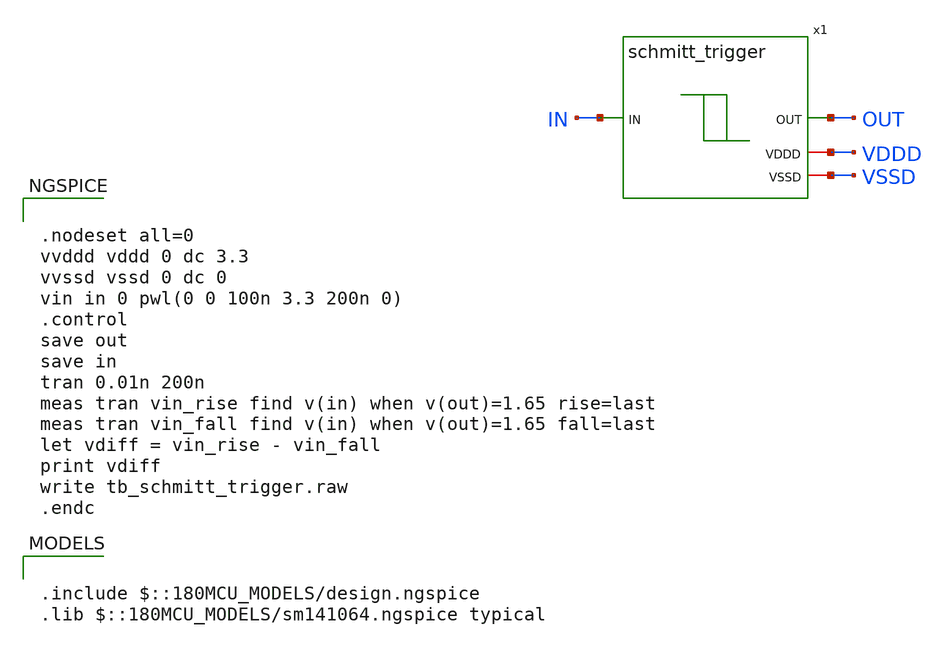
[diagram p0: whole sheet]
** sch_path: designs/libs/tb_switch_matrix/tb_schmitt_trigger.sch
**.subckt tb_schmitt_trigger
x1 IN OUT VDDD VSSD schmitt_trigger
**** begin user architecture code

.include $::180MCU_MODELS/design.ngspice
.lib $::180MCU_MODELS/sm141064.ngspice typical



.nodeset all=0
vvddd vddd 0 dc 3.3
vvssd vssd 0 dc 0
vin in 0 pwl(0 0 100n 3.3 200n 0)
.control
save out
save in
tran 0.01n 200n
meas tran vin_rise find v(in) when v(out)=1.65 rise=last
meas tran vin_fall find v(in) when v(out)=1.65 fall=last
let vdiff = vin_rise - vin_fall
print vdiff
write tb_schmitt_trigger.raw
.endc


**** end user architecture code
**.ends

* expanding   symbol:  libs/core_switch_matrix/schmitt_trigger/schmitt_trigger.sym # of pins=4
** sym_path: designs/libs/core_switch_matrix/schmitt_trigger/schmitt_trigger.sym
** sch_path: designs/libs/core_switch_matrix/schmitt_trigger/schmitt_trigger.sch
.subckt schmitt_trigger IN OUT VDDD VSSD
*.ipin IN
*.opin OUT
*.iopin VDDD
*.iopin VSSD
XM1 net1 IN VSSD VSSD nfet_03v3 L=0.28u W=0.5u nf=1 ad='int((nf+1)/2) * W/nf * 0.18u' as='int((nf+2)/2) * W/nf * 0.18u'
+ pd='2*int((nf+1)/2) * (W/nf + 0.18u)' ps='2*int((nf+2)/2) * (W/nf + 0.18u)' nrd='0.18u / W' nrs='0.18u / W'
+ sa=0 sb=0 sd=0 m=12
XM2 net2 IN net1 VSSD nfet_03v3 L=0.28u W=0.5u nf=1 ad='int((nf+1)/2) * W/nf * 0.18u' as='int((nf+2)/2) * W/nf * 0.18u'
+ pd='2*int((nf+1)/2) * (W/nf + 0.18u)' ps='2*int((nf+2)/2) * (W/nf + 0.18u)' nrd='0.18u / W' nrs='0.18u / W'
+ sa=0 sb=0 sd=0 m=12
XM3 VDDD net2 net1 VSSD nfet_03v3 L=0.56u W=0.5u nf=1 ad='int((nf+1)/2) * W/nf * 0.18u' as='int((nf+2)/2) * W/nf * 0.18u'
+ pd='2*int((nf+1)/2) * (W/nf + 0.18u)' ps='2*int((nf+2)/2) * (W/nf + 0.18u)' nrd='0.18u / W' nrs='0.18u / W'
+ sa=0 sb=0 sd=0 m=1
XM4 net3 IN VDDD VDDD pfet_03v3 L=0.28u W=1.5u nf=1 ad='int((nf+1)/2) * W/nf * 0.18u' as='int((nf+2)/2) * W/nf * 0.18u'
+ pd='2*int((nf+1)/2) * (W/nf + 0.18u)' ps='2*int((nf+2)/2) * (W/nf + 0.18u)' nrd='0.18u / W' nrs='0.18u / W'
+ sa=0 sb=0 sd=0 m=12
XM5 net2 IN net3 VDDD pfet_03v3 L=0.28u W=1.5u nf=1 ad='int((nf+1)/2) * W/nf * 0.18u' as='int((nf+2)/2) * W/nf * 0.18u'
+ pd='2*int((nf+1)/2) * (W/nf + 0.18u)' ps='2*int((nf+2)/2) * (W/nf + 0.18u)' nrd='0.18u / W' nrs='0.18u / W'
+ sa=0 sb=0 sd=0 m=12
XM6 VSSD net2 net3 VDDD pfet_03v3 L=0.56u W=1.5u nf=1 ad='int((nf+1)/2) * W/nf * 0.18u' as='int((nf+2)/2) * W/nf * 0.18u'
+ pd='2*int((nf+1)/2) * (W/nf + 0.18u)' ps='2*int((nf+2)/2) * (W/nf + 0.18u)' nrd='0.18u / W' nrs='0.18u / W'
+ sa=0 sb=0 sd=0 m=1
XM7 OUT net2 VSSD VSSD nfet_03v3 L=0.28u W=0.5u nf=1 ad='int((nf+1)/2) * W/nf * 0.18u' as='int((nf+2)/2) * W/nf * 0.18u'
+ pd='2*int((nf+1)/2) * (W/nf + 0.18u)' ps='2*int((nf+2)/2) * (W/nf + 0.18u)' nrd='0.18u / W' nrs='0.18u / W'
+ sa=0 sb=0 sd=0 m=2
XM8 OUT net2 VDDD VDDD pfet_03v3 L=0.28u W=1.5u nf=1 ad='int((nf+1)/2) * W/nf * 0.18u' as='int((nf+2)/2) * W/nf * 0.18u'
+ pd='2*int((nf+1)/2) * (W/nf + 0.18u)' ps='2*int((nf+2)/2) * (W/nf + 0.18u)' nrd='0.18u / W' nrs='0.18u / W'
+ sa=0 sb=0 sd=0 m=2
.ends

.end
